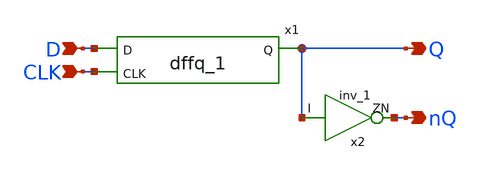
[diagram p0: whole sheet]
** sch_path: DAC/xschem/std_cell/dffqnq_1.sch
**.subckt dffqnq_1 D CLK Q nQ
*.ipin D
*.ipin CLK
*.opin Q
*.opin nQ
x1 D CLK Q VDD VNW VPW VSS gf180mcu_fd_sc_mcu7t5v0__dffq_1
x2 Q nQ VDD VNW VPW VSS gf180mcu_fd_sc_mcu7t5v0__inv_1
**.ends
.end
